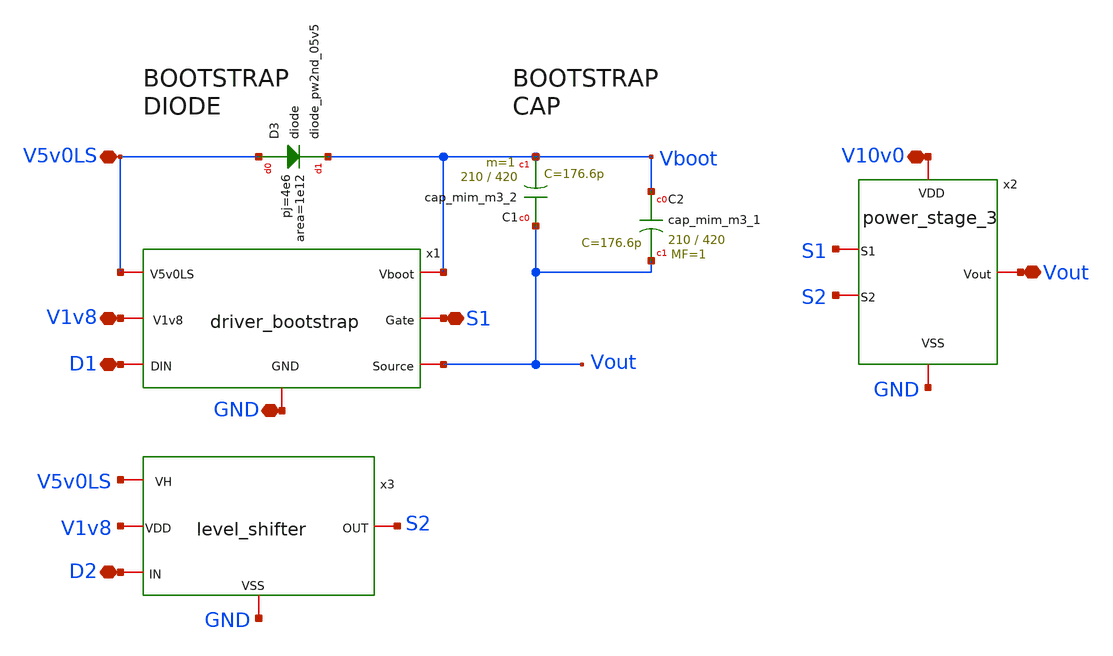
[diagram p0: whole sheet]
** sch_path: xschem/converter_3.sch
**.subckt converter_3 V5v0LS V1v8 GND D1 S1 Vout V10v0 D2
*.iopin V5v0LS
*.iopin V1v8
*.iopin GND
*.iopin D1
*.iopin S1
*.iopin Vout
*.iopin V10v0
*.iopin D2
x1 Vboot S1 Vout V5v0LS V1v8 GND D1 driver_bootstrap
XD3 V5v0LS Vboot sky130_fd_pr__diode_pw2nd_05v5 area=1e12 pj=4e6
XC1 Vout Vboot sky130_fd_pr__cap_mim_m3_2 W=210 L=420 MF=1 m=1
x2 V10v0 S1 Vout S2 GND power_stage_3
x3 V5v0LS V1v8 S2 D2 GND level_shifter
XC2 Vboot Vout sky130_fd_pr__cap_mim_m3_1 W=210 L=420 MF=1 m=1
**.ends
.end
